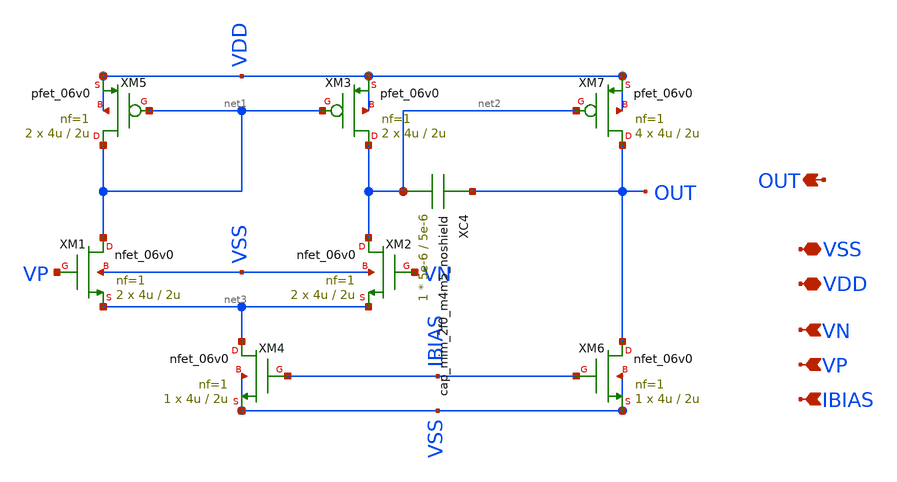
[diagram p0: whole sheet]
** sch_path: designs/libs/core_n-ota/n-ota-6v/n-ota.sch
**.subckt n-ota VN VP OUT VDD VSS IBIAS
*.ipin VN
*.ipin VP
*.opin OUT
*.iopin VDD
*.iopin VSS
*.ipin IBIAS
XM1 net1 VP net3 VSS nfet_06v0 L=2u W=4u nf=1 ad='int((nf+1)/2) * W/nf * 0.18u' as='int((nf+2)/2) * W/nf * 0.18u'
+ pd='2*int((nf+1)/2) * (W/nf + 0.18u)' ps='2*int((nf+2)/2) * (W/nf + 0.18u)' nrd='0.18u / W' nrs='0.18u / W'
+ sa=0 sb=0 sd=0 m=2
XM2 net2 VN net3 VSS nfet_06v0 L=2u W=4u nf=1 ad='int((nf+1)/2) * W/nf * 0.18u' as='int((nf+2)/2) * W/nf * 0.18u'
+ pd='2*int((nf+1)/2) * (W/nf + 0.18u)' ps='2*int((nf+2)/2) * (W/nf + 0.18u)' nrd='0.18u / W' nrs='0.18u / W'
+ sa=0 sb=0 sd=0 m=2
XM4 net3 IBIAS VSS VSS nfet_06v0 L=2u W=4u nf=1 ad='int((nf+1)/2) * W/nf * 0.18u' as='int((nf+2)/2) * W/nf * 0.18u'
+ pd='2*int((nf+1)/2) * (W/nf + 0.18u)' ps='2*int((nf+2)/2) * (W/nf + 0.18u)' nrd='0.18u / W' nrs='0.18u / W'
+ sa=0 sb=0 sd=0 m=1
XM3 net2 net1 VDD VDD pfet_06v0 L=2u W=4u nf=1 ad='int((nf+1)/2) * W/nf * 0.18u' as='int((nf+2)/2) * W/nf * 0.18u'
+ pd='2*int((nf+1)/2) * (W/nf + 0.18u)' ps='2*int((nf+2)/2) * (W/nf + 0.18u)' nrd='0.18u / W' nrs='0.18u / W'
+ sa=0 sb=0 sd=0 m=2
XM5 net1 net1 VDD VDD pfet_06v0 L=2u W=4u nf=1 ad='int((nf+1)/2) * W/nf * 0.18u' as='int((nf+2)/2) * W/nf * 0.18u'
+ pd='2*int((nf+1)/2) * (W/nf + 0.18u)' ps='2*int((nf+2)/2) * (W/nf + 0.18u)' nrd='0.18u / W' nrs='0.18u / W'
+ sa=0 sb=0 sd=0 m=2
XM6 OUT IBIAS VSS VSS nfet_06v0 L=2u W=4u nf=1 ad='int((nf+1)/2) * W/nf * 0.18u' as='int((nf+2)/2) * W/nf * 0.18u'
+ pd='2*int((nf+1)/2) * (W/nf + 0.18u)' ps='2*int((nf+2)/2) * (W/nf + 0.18u)' nrd='0.18u / W' nrs='0.18u / W'
+ sa=0 sb=0 sd=0 m=1
XM7 OUT net2 VDD VDD pfet_06v0 L=2u W=4u nf=1 ad='int((nf+1)/2) * W/nf * 0.18u' as='int((nf+2)/2) * W/nf * 0.18u'
+ pd='2*int((nf+1)/2) * (W/nf + 0.18u)' ps='2*int((nf+2)/2) * (W/nf + 0.18u)' nrd='0.18u / W' nrs='0.18u / W'
+ sa=0 sb=0 sd=0 m=4
XC4 OUT net2 cap_mim_2f0_m4m5_noshield c_width=5e-6 c_length=5e-6 m=1
**.ends
.end
